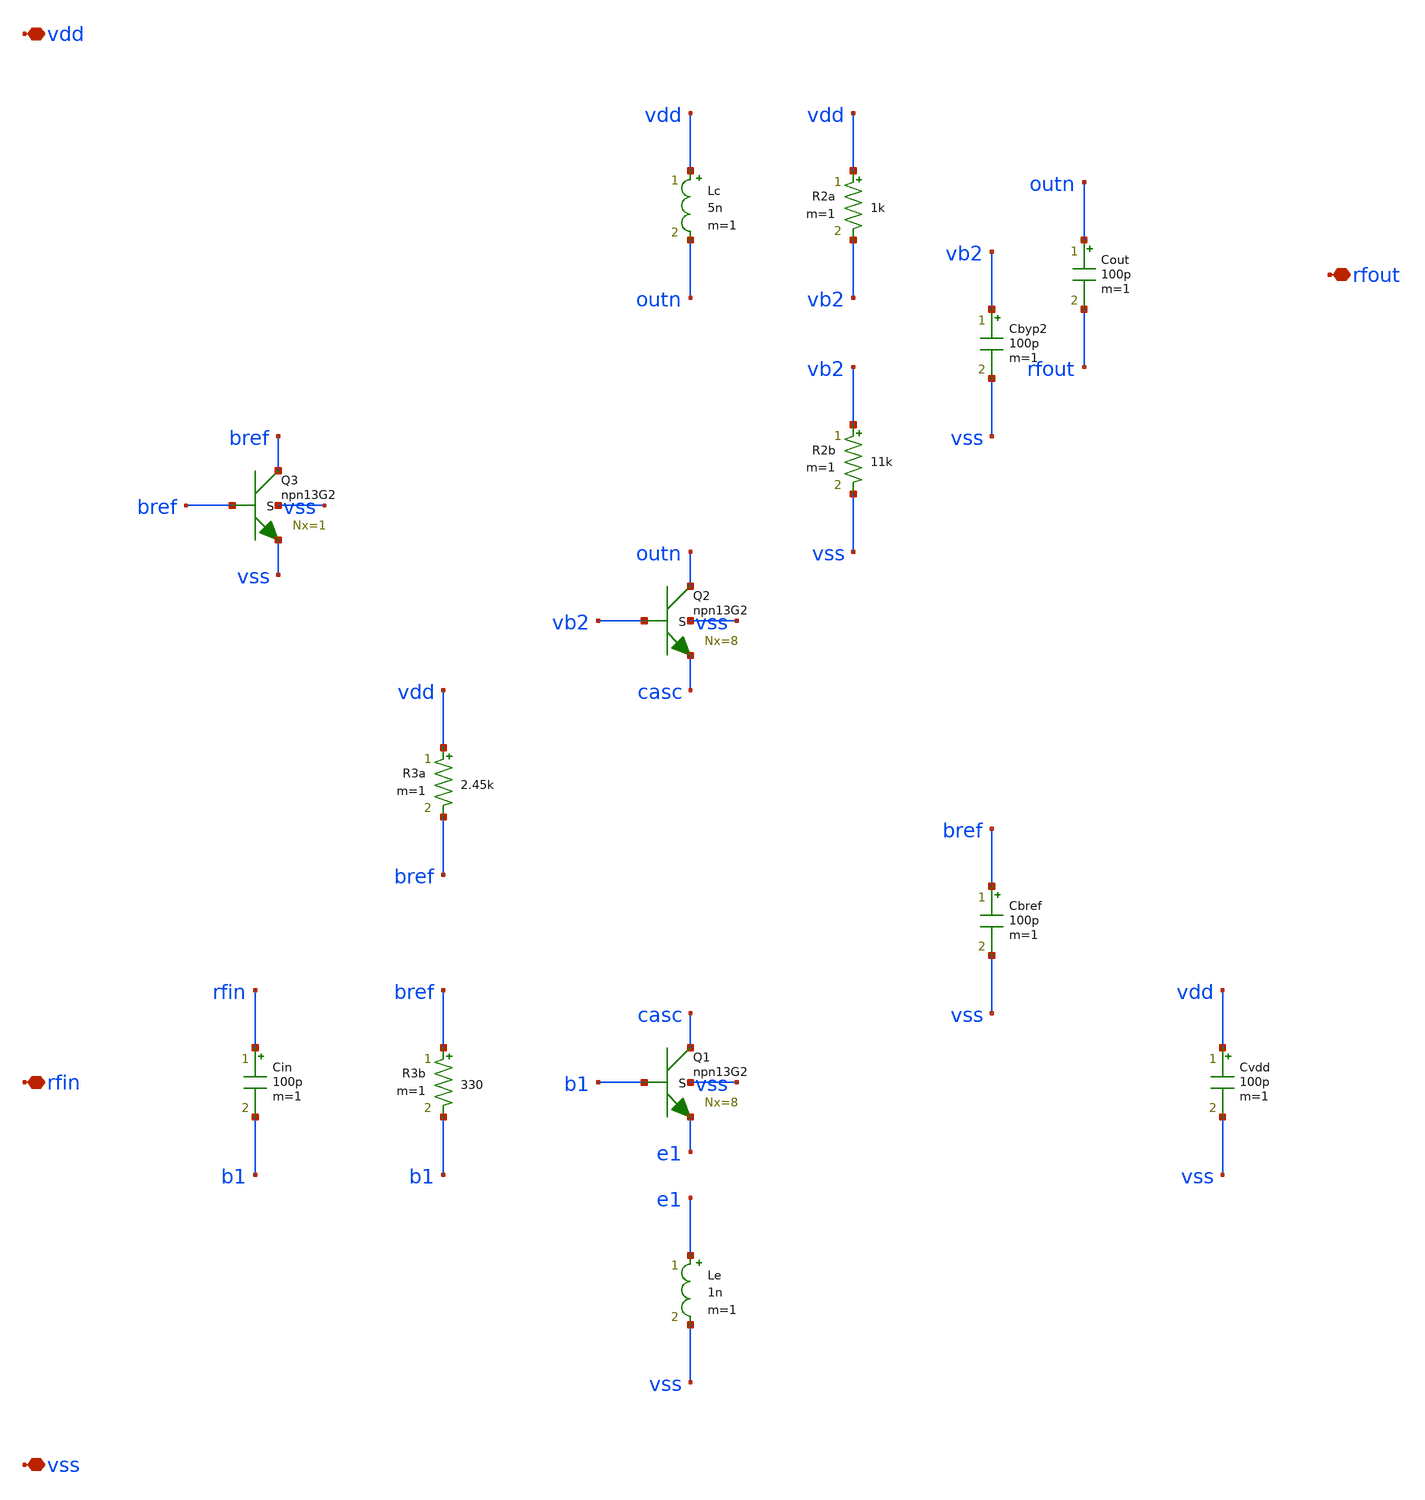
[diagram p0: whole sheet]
** sch_path: design/lna.sch
**.subckt lna vdd vss rfin rfout
*.iopin vdd
*.iopin vss
*.iopin rfin
*.iopin rfout
XQ2 outn vb2 casc vss npn13G2 Nx=8 mm_ok=1
XQ1 casc b1 e1 vss npn13G2 Nx=8 mm_ok=1
Le e1 vss 1n m=1
Lc vdd outn 5n m=1
Cin rfin b1 100p m=1
Cout outn rfout 100p m=1
Cbyp2 vb2 vss 100p m=1
Cvdd vdd vss 100p m=1
R2a vdd vb2 1k m=1
R2b vb2 vss 11k m=1
R3a vdd bref 2.45k m=1
R3b bref b1 330 m=1
XQ3 bref bref vss vss npn13G2 Nx=1 mm_ok=1
Cbref bref vss 100p m=1
**.ends
.end
